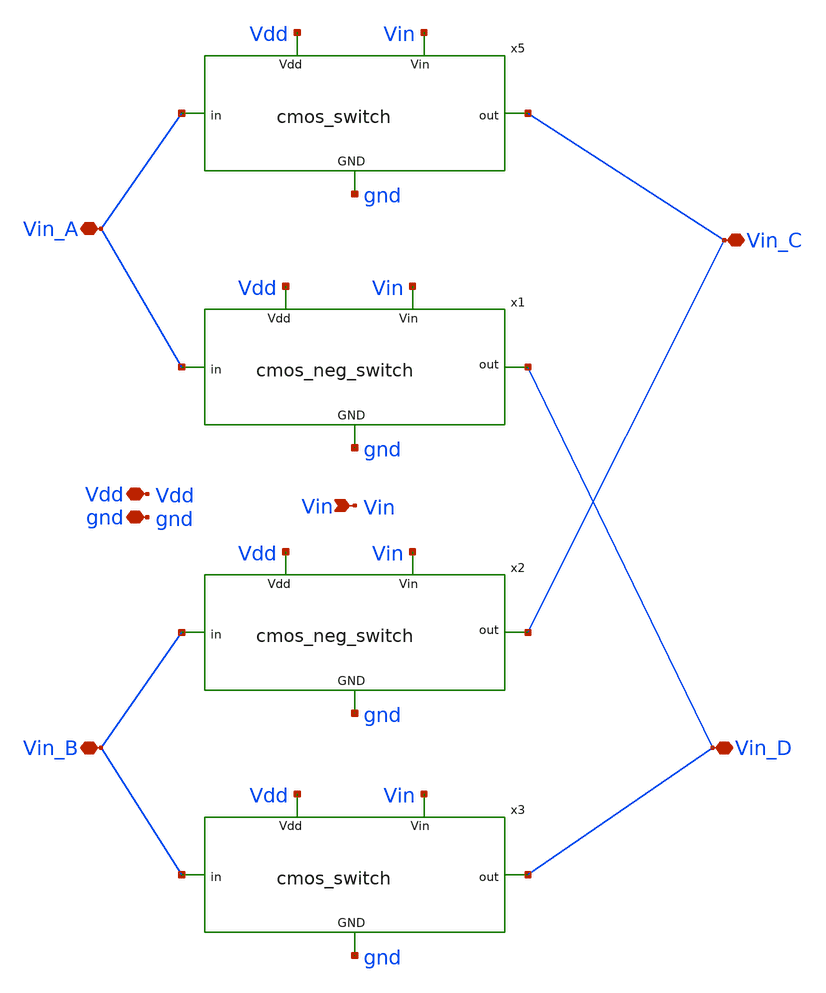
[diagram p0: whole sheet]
** sch_path: MRTMOS_final_chip/cmos_cross_switch.sch
**.subckt cmos_cross_switch Vin Vin_A Vin_B Vin_C Vin_D Vdd gnd
*.ipin Vin
*.iopin Vin_A
*.iopin Vin_B
*.iopin Vin_C
*.iopin Vin_D
*.iopin Vdd
*.iopin gnd
x5 Vdd Vin_A Vin gnd Vin_C cmos_switch
x3 Vdd Vin_B Vin gnd Vin_D cmos_switch
x1 Vdd Vin_A Vin gnd Vin_D cmos_neg_switch
x2 Vdd Vin_B Vin gnd Vin_C cmos_neg_switch
**.ends

* expanding   symbol:  MG_switch/cmos_switch.sym # of pins=5
** sym_path: MRTMOS_final_chip/cmos_switch.sym
** sch_path: MRTMOS_final_chip/cmos_switch.sch
.subckt cmos_switch Vdd in Vin GND out
*.ipin Vdd
*.ipin Vin
*.ipin in
*.ipin out
*.ipin GND
XM1 in Vin out GND nfet_05v0 L=0.7u W=2u nf=2 ad='int((nf+1)/2) * W/nf * 0.18u' as='int((nf+2)/2) * W/nf * 0.18u'
+ pd='2*int((nf+1)/2) * (W/nf + 0.18u)' ps='2*int((nf+2)/2) * (W/nf + 0.18u)' nrd='0.18u / W' nrs='0.18u / W'
+ sa=0 sb=0 sd=0 m=1
XM2 out net1 in Vdd pfet_05v0 L=0.7u W=6u nf=6 ad='int((nf+1)/2) * W/nf * 0.18u' as='int((nf+2)/2) * W/nf * 0.18u'
+ pd='2*int((nf+1)/2) * (W/nf + 0.18u)' ps='2*int((nf+2)/2) * (W/nf + 0.18u)' nrd='0.18u / W' nrs='0.18u / W'
+ sa=0 sb=0 sd=0 m=1
XM3 net1 Vin GND GND nfet_05v0 L=0.7u W=1u nf=1 ad='int((nf+1)/2) * W/nf * 0.18u' as='int((nf+2)/2) * W/nf * 0.18u'
+ pd='2*int((nf+1)/2) * (W/nf + 0.18u)' ps='2*int((nf+2)/2) * (W/nf + 0.18u)' nrd='0.18u / W' nrs='0.18u / W'
+ sa=0 sb=0 sd=0 m=1
XM4 net1 Vin Vdd Vdd pfet_05v0 L=0.7u W=3u nf=2 ad='int((nf+1)/2) * W/nf * 0.18u' as='int((nf+2)/2) * W/nf * 0.18u'
+ pd='2*int((nf+1)/2) * (W/nf + 0.18u)' ps='2*int((nf+2)/2) * (W/nf + 0.18u)' nrd='0.18u / W' nrs='0.18u / W'
+ sa=0 sb=0 sd=0 m=1
XC3 Vdd GND cap_nmos_06v0 c_width=60e-6 c_length=10e-6 m=6
.ends


* expanding   symbol:  MG_switch/cmos_neg_switch.sym # of pins=5
** sym_path: MG_switch/cmos_neg_switch.sym
** sch_path: MG_switch/cmos_neg_switch.sch
.subckt cmos_neg_switch Vdd in Vin GND out
*.ipin Vdd
*.ipin Vin
*.ipin in
*.ipin out
*.ipin GND
XM1 in net1 out GND nfet_05v0 L=0.7u W=2u nf=2 ad='int((nf+1)/2) * W/nf * 0.18u' as='int((nf+2)/2) * W/nf * 0.18u'
+ pd='2*int((nf+1)/2) * (W/nf + 0.18u)' ps='2*int((nf+2)/2) * (W/nf + 0.18u)' nrd='0.18u / W' nrs='0.18u / W'
+ sa=0 sb=0 sd=0 m=1
XM2 out Vin in Vdd pfet_05v0 L=0.7u W=6u nf=6 ad='int((nf+1)/2) * W/nf * 0.18u' as='int((nf+2)/2) * W/nf * 0.18u'
+ pd='2*int((nf+1)/2) * (W/nf + 0.18u)' ps='2*int((nf+2)/2) * (W/nf + 0.18u)' nrd='0.18u / W' nrs='0.18u / W'
+ sa=0 sb=0 sd=0 m=1
XM3 net1 Vin GND GND nfet_05v0 L=0.7u W=1u nf=1 ad='int((nf+1)/2) * W/nf * 0.18u' as='int((nf+2)/2) * W/nf * 0.18u'
+ pd='2*int((nf+1)/2) * (W/nf + 0.18u)' ps='2*int((nf+2)/2) * (W/nf + 0.18u)' nrd='0.18u / W' nrs='0.18u / W'
+ sa=0 sb=0 sd=0 m=1
XM4 net1 Vin Vdd Vdd pfet_05v0 L=0.7u W=2.2u nf=1 ad='int((nf+1)/2) * W/nf * 0.18u' as='int((nf+2)/2) * W/nf * 0.18u'
+ pd='2*int((nf+1)/2) * (W/nf + 0.18u)' ps='2*int((nf+2)/2) * (W/nf + 0.18u)' nrd='0.18u / W' nrs='0.18u / W'
+ sa=0 sb=0 sd=0 m=1
XC3 Vdd GND cap_nmos_06v0 c_width=30e-6 c_length=30e-6 m=1
.ends

.end
